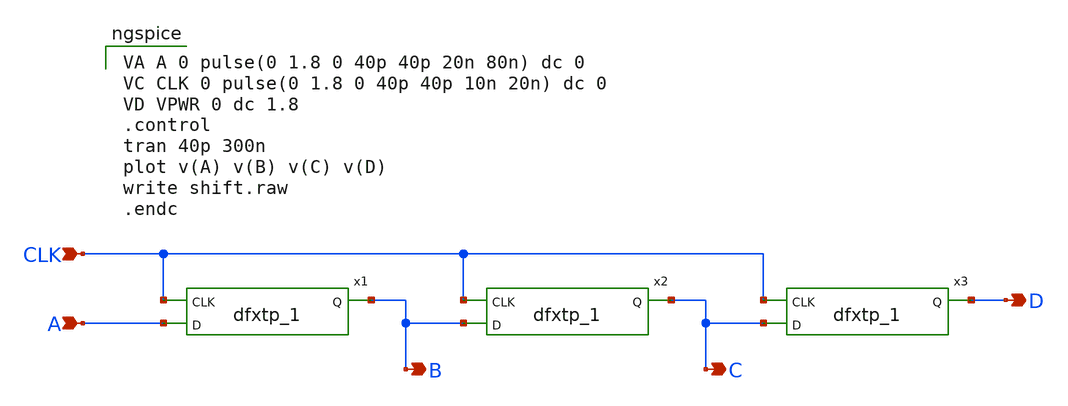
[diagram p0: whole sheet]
** sch_path: shift.sch
**.subckt shift B A C D CLK
*.opin B
*.ipin A
*.opin C
*.opin D
*.ipin CLK
x1 CLK A 0 0 VPWR VPWR B sky130_fd_sc_hd__dfxtp_1
x2 CLK B 0 0 VPWR VPWR C sky130_fd_sc_hd__dfxtp_1
x3 CLK C 0 0 VPWR VPWR D sky130_fd_sc_hd__dfxtp_1
**** begin user architecture code

VA A 0 pulse(0 1.8 0 40p 40p 20n 80n) dc 0
VC CLK 0 pulse(0 1.8 0 40p 40p 10n 20n) dc 0
VD VPWR 0 dc 1.8
.control
tran 40p 300n
plot v(A) v(B) v(C) v(D)
write shift.raw
.endc


** opencircuitdesign pdks install
.lib $::SKYWATER_MODELS/sky130.lib.spice tt
.include $::SKYWATER_STDCELLS/sky130_fd_sc_hd.spice

**** end user architecture code
**.ends
.end
